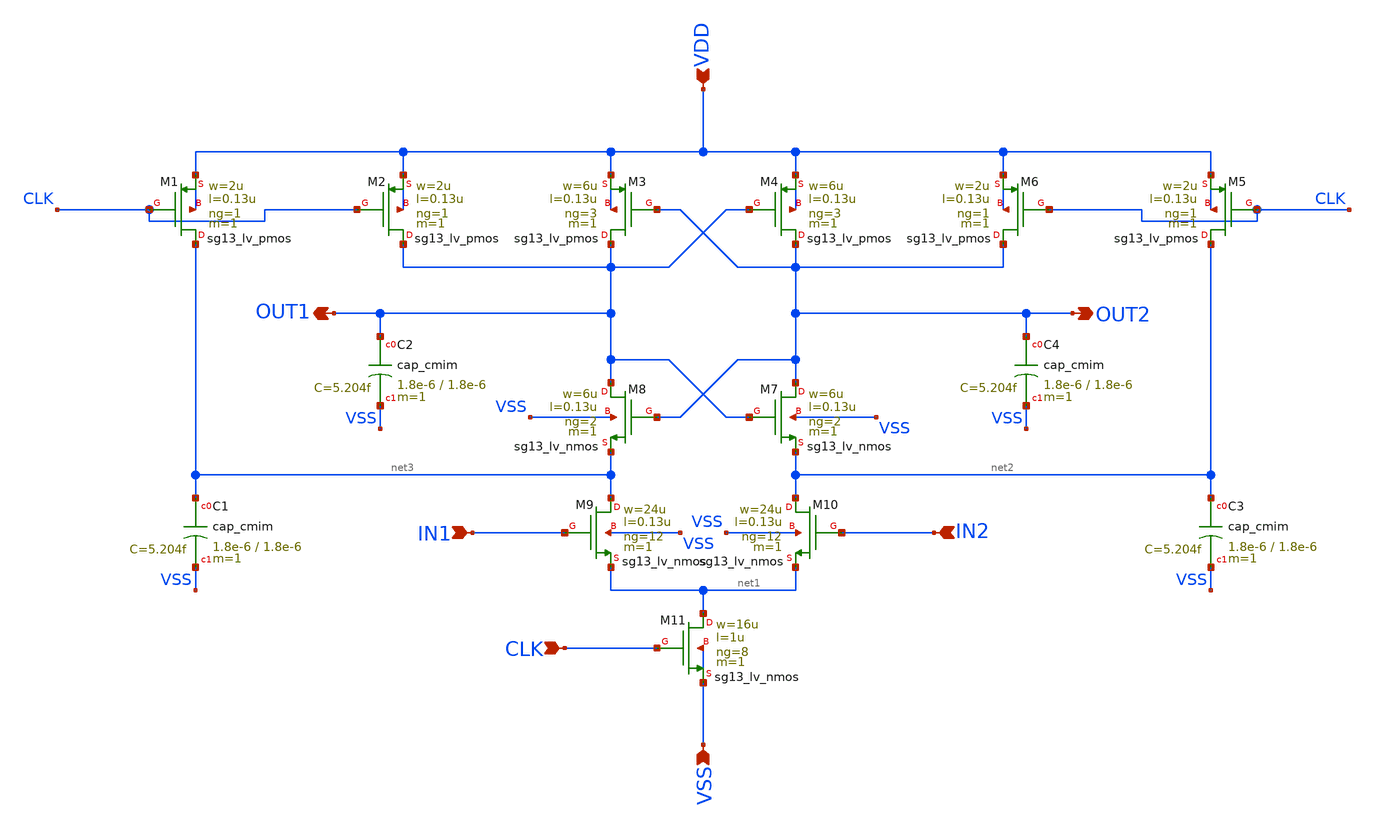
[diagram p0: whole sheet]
** sch_path: designs/comparator/comparator_old.sch
**.subckt comparator_old CLK IN1 IN2 OUT2 OUT1 VSS VDD
*.ipin CLK
*.ipin IN1
*.ipin IN2
*.opin OUT2
*.opin OUT1
*.ipin VSS
*.ipin VDD
XM1 net3 CLK VDD VDD sg13_lv_pmos w=2u l=0.13u ng=1 m=1 mm_ok=1
XM3 OUT1 OUT2 VDD VDD sg13_lv_pmos w=6u l=0.13u ng=3 m=1 mm_ok=1
XM4 OUT2 OUT1 VDD VDD sg13_lv_pmos w=6u l=0.13u ng=3 m=1 mm_ok=1
XM8 OUT1 OUT2 net3 VSS sg13_lv_nmos w=6u l=0.13u ng=2 m=1 mm_ok=1
XM9 net3 IN1 net1 VSS sg13_lv_nmos w=24u l=0.13u ng=12 m=1 mm_ok=1
XM11 net1 CLK VSS VSS sg13_lv_nmos w=16u l=1u ng=8 m=1 mm_ok=1
XM10 net2 IN2 net1 VSS sg13_lv_nmos w=24u l=0.13u ng=12 m=1 mm_ok=1
XM2 OUT1 CLK VDD VDD sg13_lv_pmos w=2u l=0.13u ng=1 m=1 mm_ok=1
XM5 net2 CLK VDD VDD sg13_lv_pmos w=2u l=0.13u ng=1 m=1 mm_ok=1
XM6 OUT2 CLK VDD VDD sg13_lv_pmos w=2u l=0.13u ng=1 m=1 mm_ok=1
XM7 OUT2 OUT1 net2 VSS sg13_lv_nmos w=6u l=0.13u ng=2 m=1 mm_ok=1
XC1 net3 VSS cap_cmim w=1.8e-6 l=1.8e-6 m=1 mm_ok=1
XC2 OUT1 VSS cap_cmim w=1.8e-6 l=1.8e-6 m=1 mm_ok=1
XC3 net2 VSS cap_cmim w=1.8e-6 l=1.8e-6 m=1 mm_ok=1
XC4 OUT2 VSS cap_cmim w=1.8e-6 l=1.8e-6 m=1 mm_ok=1
**.ends
.end
